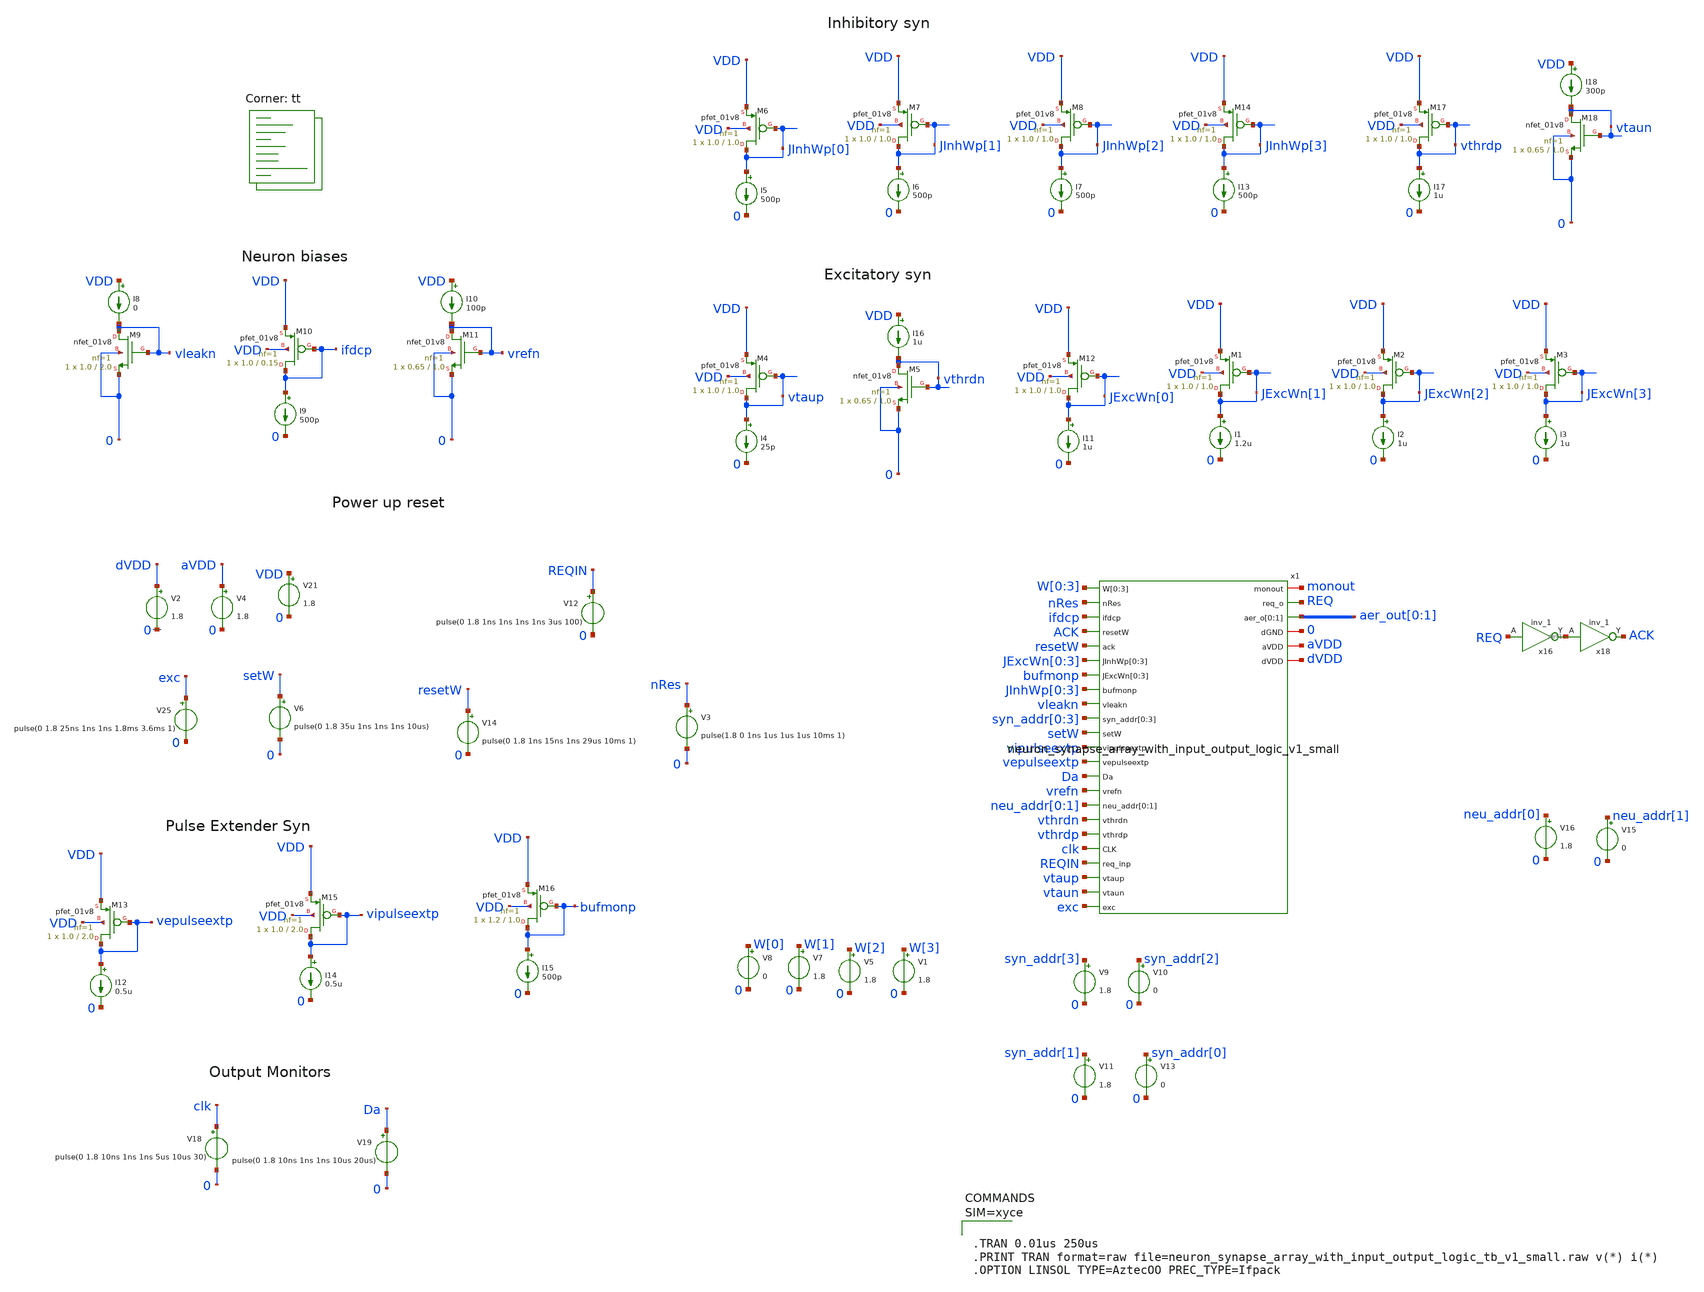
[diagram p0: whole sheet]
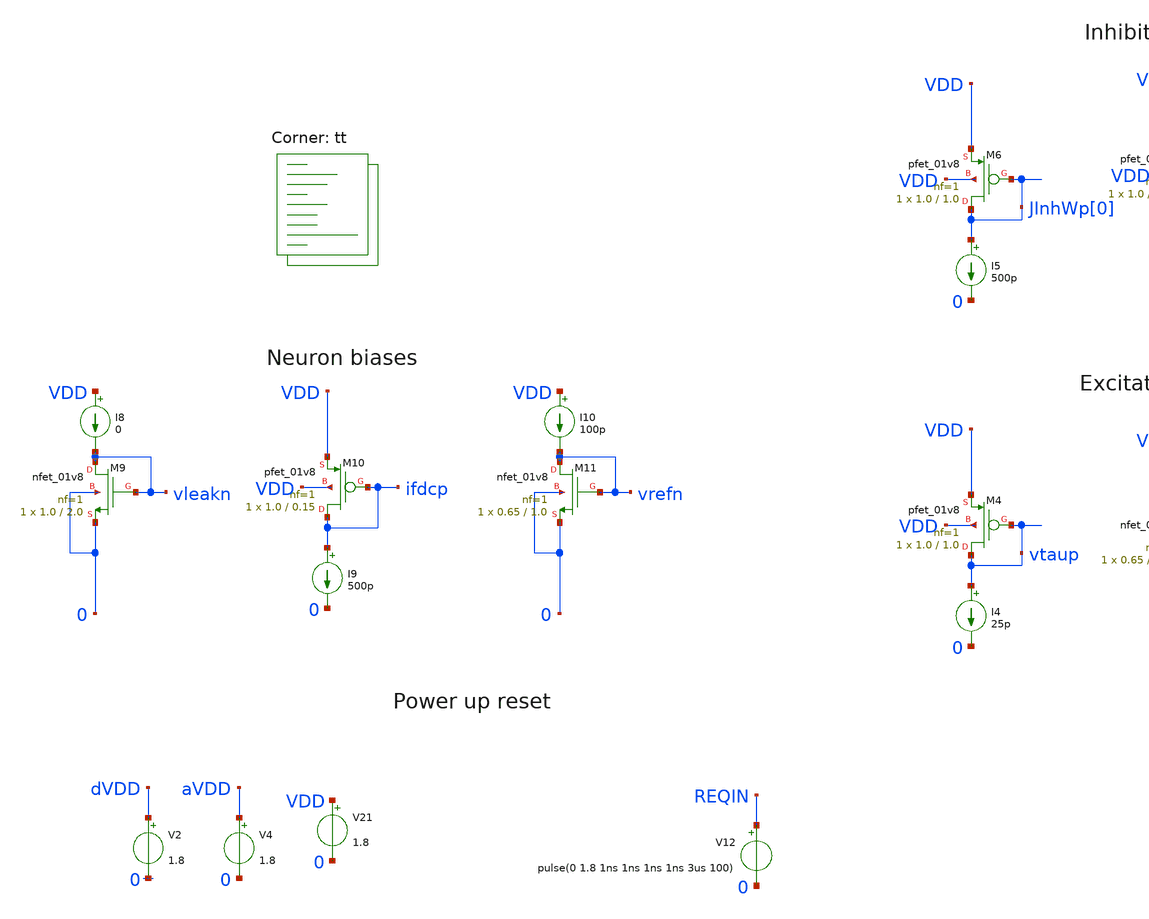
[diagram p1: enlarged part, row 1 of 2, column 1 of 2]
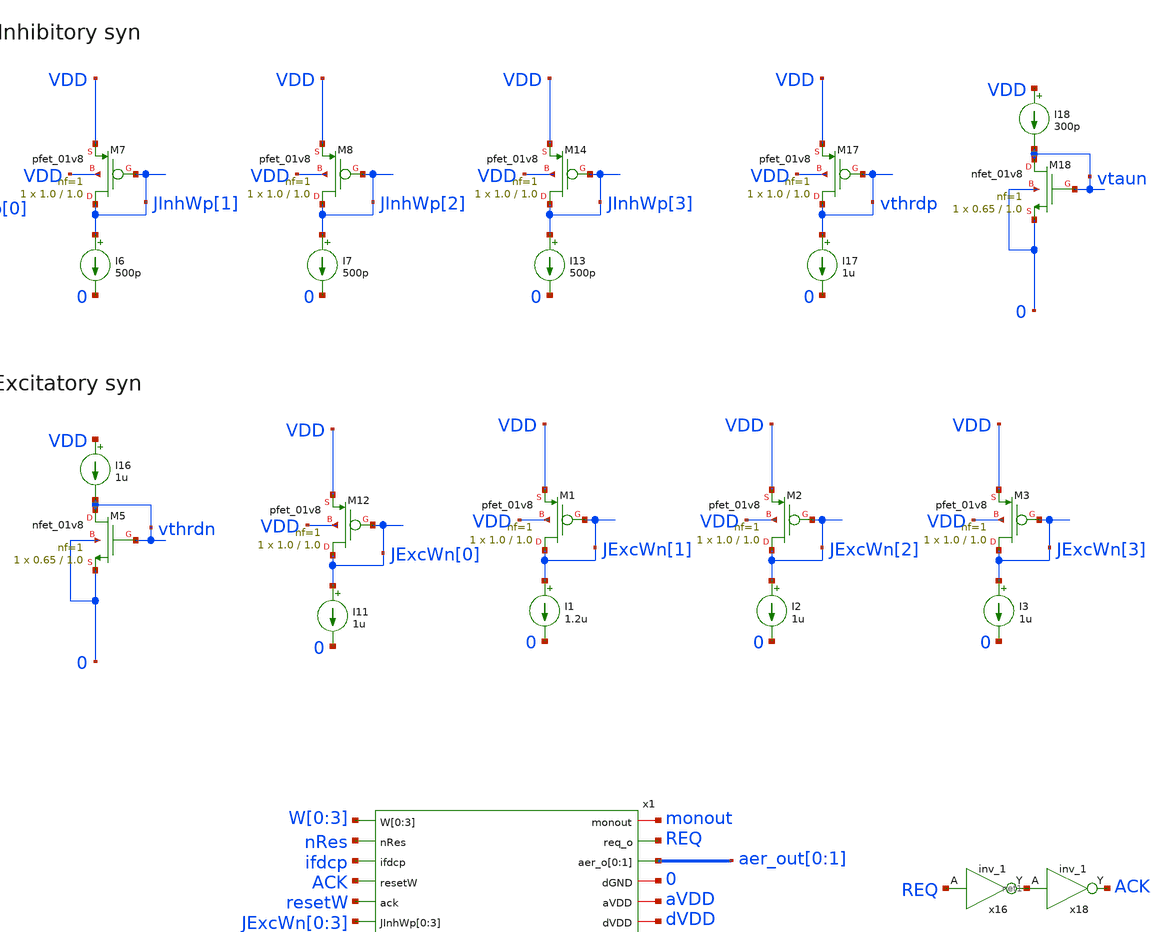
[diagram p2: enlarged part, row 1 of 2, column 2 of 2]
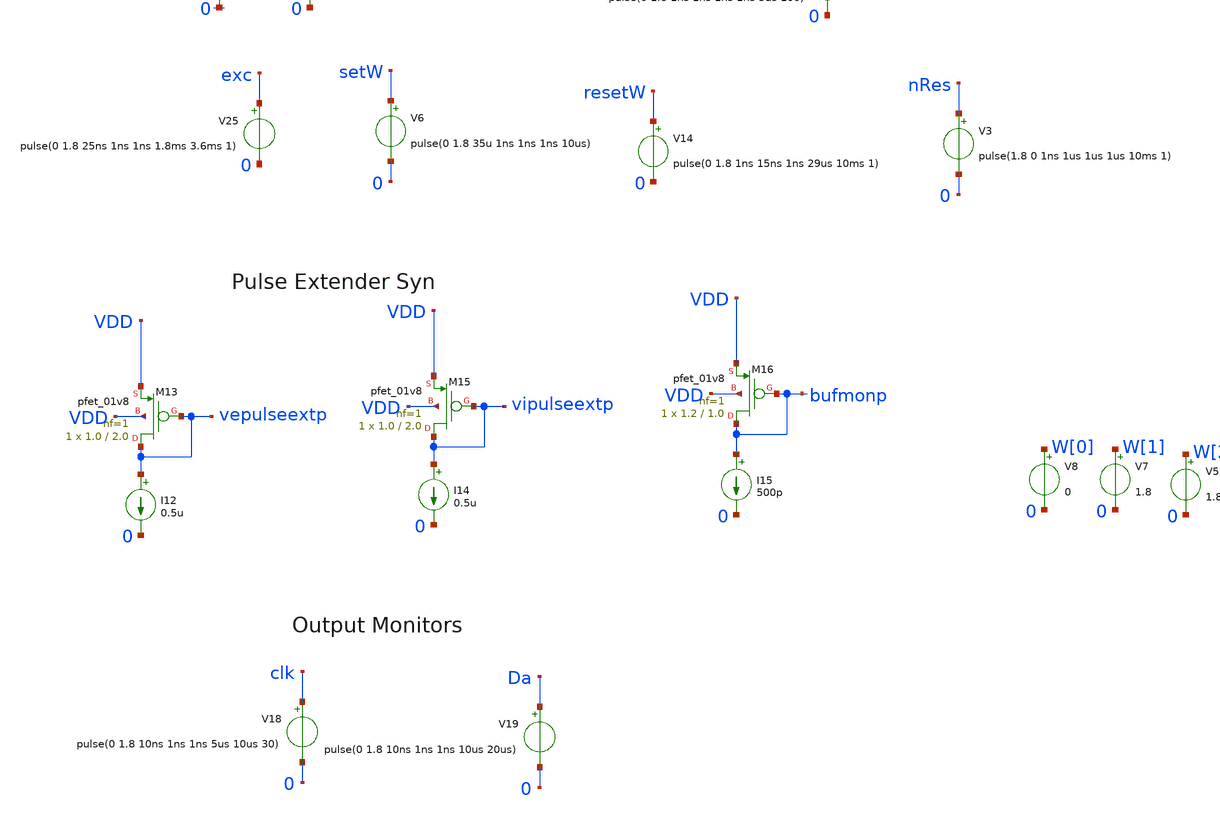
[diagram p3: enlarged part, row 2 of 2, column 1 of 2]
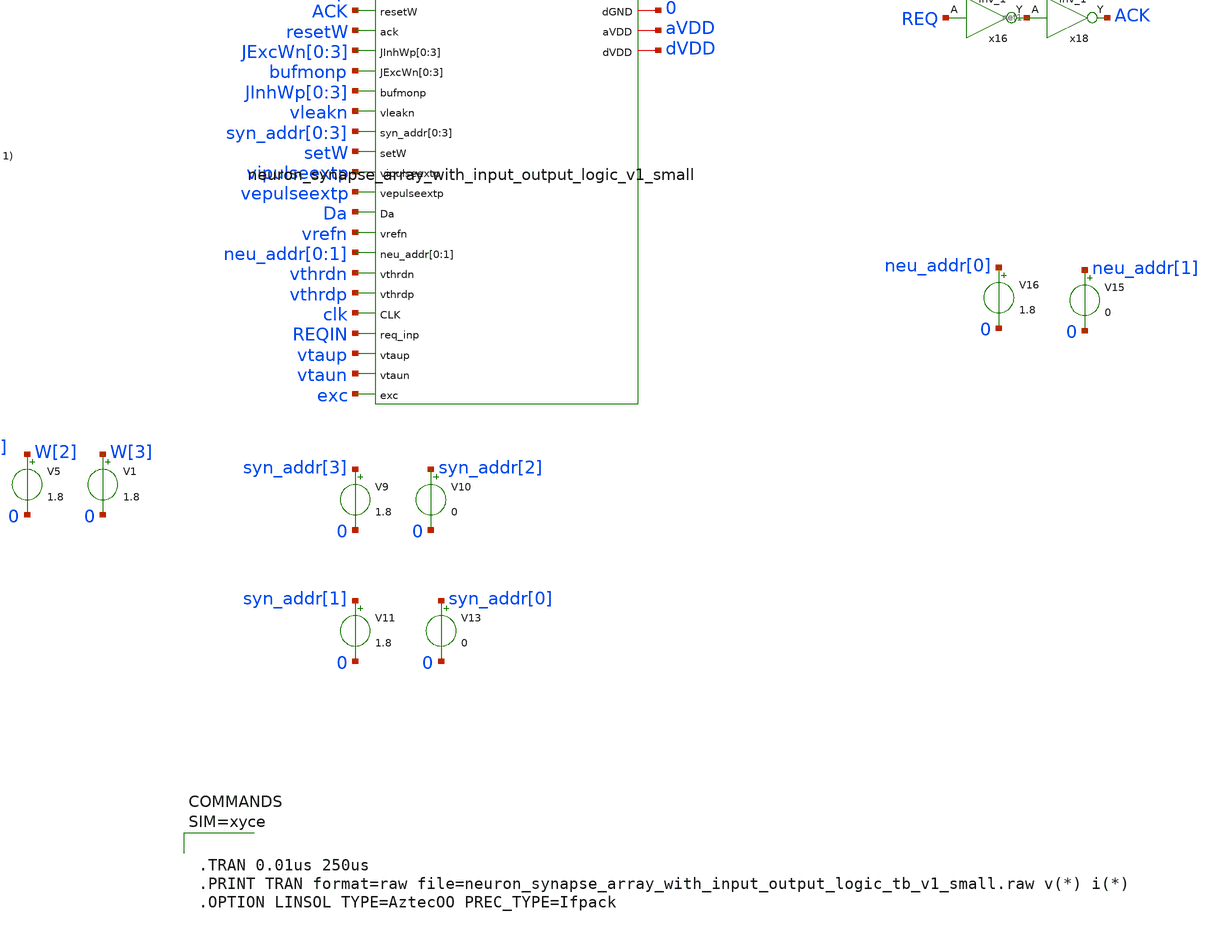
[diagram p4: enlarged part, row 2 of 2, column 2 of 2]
** sch_path: design/xschem/neuron_synapse_array_with_input_output_logic_v1_small_tb.sch
**.subckt neuron_synapse_array_with_input_output_logic_v1_small_tb
V2 dVDD 0 1.8
V12 REQIN 0 pulse(0 1.8 1ns 1ns 1ns 1ns 3us 100)
V4 aVDD 0 1.8
x16 REQ 0 0 VDD VDD net1 sky130_fd_sc_hd__inv_1
x18 net1 0 0 VDD VDD ACK sky130_fd_sc_hd__inv_1
V21 VDD 0 1.8
I8 VDD vleakn 0
XM9 vleakn vleakn 0 0 sky130_fd_pr__nfet_01v8 L=2.0 W=1.0 nf=1 ad='int((nf+1)/2) * W/nf * 0.29' as='int((nf+2)/2) * W/nf * 0.29'
+ pd='2*int((nf+1)/2) * (W/nf + 0.29)' ps='2*int((nf+2)/2) * (W/nf + 0.29)' nrd='0.29 / W' nrs='0.29 / W'
+ sa=0 sb=0 sd=0 mult=1 m=1
XM10 ifdcp ifdcp VDD VDD sky130_fd_pr__pfet_01v8 L=0.15 W=1.0 nf=1 ad='int((nf+1)/2) * W/nf * 0.29' as='int((nf+2)/2) * W/nf * 0.29'
+ pd='2*int((nf+1)/2) * (W/nf + 0.29)' ps='2*int((nf+2)/2) * (W/nf + 0.29)' nrd='0.29 / W' nrs='0.29 / W'
+ sa=0 sb=0 sd=0 mult=1 m=1
I9 ifdcp 0 500p
I10 VDD vrefn 100p
XM11 vrefn vrefn 0 0 sky130_fd_pr__nfet_01v8 L=1.0 W=0.65 nf=1 ad='int((nf+1)/2) * W/nf * 0.29' as='int((nf+2)/2) * W/nf * 0.29'
+ pd='2*int((nf+1)/2) * (W/nf + 0.29)' ps='2*int((nf+2)/2) * (W/nf + 0.29)' nrd='0.29 / W' nrs='0.29 / W'
+ sa=0 sb=0 sd=0 mult=1 m=1
XM13 vepulseextp vepulseextp VDD VDD sky130_fd_pr__pfet_01v8 L=2.0 W=1.0 nf=1 ad='int((nf+1)/2) * W/nf * 0.29'
+ as='int((nf+2)/2) * W/nf * 0.29' pd='2*int((nf+1)/2) * (W/nf + 0.29)' ps='2*int((nf+2)/2) * (W/nf + 0.29)'
+ nrd='0.29 / W' nrs='0.29 / W' sa=0 sb=0 sd=0 mult=1 m=1
I12 vepulseextp 0 0.5u
XM15 vipulseextp vipulseextp VDD VDD sky130_fd_pr__pfet_01v8 L=2.0 W=1.0 nf=1 ad='int((nf+1)/2) * W/nf * 0.29'
+ as='int((nf+2)/2) * W/nf * 0.29' pd='2*int((nf+1)/2) * (W/nf + 0.29)' ps='2*int((nf+2)/2) * (W/nf + 0.29)'
+ nrd='0.29 / W' nrs='0.29 / W' sa=0 sb=0 sd=0 mult=1 m=1
I14 vipulseextp 0 0.5u
XM16 bufmonp bufmonp VDD VDD sky130_fd_pr__pfet_01v8 L=1.0 W=1.2 nf=1 ad='int((nf+1)/2) * W/nf * 0.29'
+ as='int((nf+2)/2) * W/nf * 0.29' pd='2*int((nf+1)/2) * (W/nf + 0.29)' ps='2*int((nf+2)/2) * (W/nf + 0.29)'
+ nrd='0.29 / W' nrs='0.29 / W' sa=0 sb=0 sd=0 mult=1 m=1
I15 bufmonp 0 500p
x1 W[0] W[1] W[2] W[3] nRes monout REQ ifdcp ACK resetW JExcWn[0] JExcWn[1] JExcWn[2] JExcWn[3]
+ aer_out[0] aer_out[1] bufmonp bufmonp bufmonp bufmonp JInhWp[0] vleakn syn_addr[0] syn_addr[1] syn_addr[2]
+ syn_addr[3] setW vipulseextp vepulseextp Da vrefn neu_addr[0] neu_addr[1] vthrdn vthrdp clk REQIN vtaup vtaun
+ exc 0 aVDD dVDD neuron_synapse_array_with_input_output_logic_v1_small
XM12 JExcWn[0] JExcWn[0] VDD VDD sky130_fd_pr__pfet_01v8 L=1.0 W=1.0 nf=1 ad='int((nf+1)/2) * W/nf * 0.29'
+ as='int((nf+2)/2) * W/nf * 0.29' pd='2*int((nf+1)/2) * (W/nf + 0.29)' ps='2*int((nf+2)/2) * (W/nf + 0.29)'
+ nrd='0.29 / W' nrs='0.29 / W' sa=0 sb=0 sd=0 mult=1 m=1
I11 JExcWn[0] 0 1u
XM1 JExcWn[1] JExcWn[1] VDD VDD sky130_fd_pr__pfet_01v8 L=1.0 W=1.0 nf=1 ad='int((nf+1)/2) * W/nf * 0.29'
+ as='int((nf+2)/2) * W/nf * 0.29' pd='2*int((nf+1)/2) * (W/nf + 0.29)' ps='2*int((nf+2)/2) * (W/nf + 0.29)'
+ nrd='0.29 / W' nrs='0.29 / W' sa=0 sb=0 sd=0 mult=1 m=1
I1 JExcWn[1] 0 1.2u
XM2 JExcWn[2] JExcWn[2] VDD VDD sky130_fd_pr__pfet_01v8 L=1.0 W=1.0 nf=1 ad='int((nf+1)/2) * W/nf * 0.29'
+ as='int((nf+2)/2) * W/nf * 0.29' pd='2*int((nf+1)/2) * (W/nf + 0.29)' ps='2*int((nf+2)/2) * (W/nf + 0.29)'
+ nrd='0.29 / W' nrs='0.29 / W' sa=0 sb=0 sd=0 mult=1 m=1
I2 JExcWn[2] 0 1u
XM3 JExcWn[3] JExcWn[3] VDD VDD sky130_fd_pr__pfet_01v8 L=1.0 W=1.0 nf=1 ad='int((nf+1)/2) * W/nf * 0.29'
+ as='int((nf+2)/2) * W/nf * 0.29' pd='2*int((nf+1)/2) * (W/nf + 0.29)' ps='2*int((nf+2)/2) * (W/nf + 0.29)'
+ nrd='0.29 / W' nrs='0.29 / W' sa=0 sb=0 sd=0 mult=1 m=1
I3 JExcWn[3] 0 1u
XM4 vtaup vtaup VDD VDD sky130_fd_pr__pfet_01v8 L=1.0 W=1.0 nf=1 ad='int((nf+1)/2) * W/nf * 0.29' as='int((nf+2)/2) * W/nf * 0.29'
+ pd='2*int((nf+1)/2) * (W/nf + 0.29)' ps='2*int((nf+2)/2) * (W/nf + 0.29)' nrd='0.29 / W' nrs='0.29 / W'
+ sa=0 sb=0 sd=0 mult=1 m=1
I4 vtaup 0 25p
I16 VDD vthrdn 1u
XM5 vthrdn vthrdn 0 0 sky130_fd_pr__nfet_01v8 L=1.0 W=0.65 nf=1 ad='int((nf+1)/2) * W/nf * 0.29' as='int((nf+2)/2) * W/nf * 0.29'
+ pd='2*int((nf+1)/2) * (W/nf + 0.29)' ps='2*int((nf+2)/2) * (W/nf + 0.29)' nrd='0.29 / W' nrs='0.29 / W'
+ sa=0 sb=0 sd=0 mult=1 m=1
XM6 JInhWp[0] JInhWp[0] VDD VDD sky130_fd_pr__pfet_01v8 L=1.0 W=1.0 nf=1 ad='int((nf+1)/2) * W/nf * 0.29'
+ as='int((nf+2)/2) * W/nf * 0.29' pd='2*int((nf+1)/2) * (W/nf + 0.29)' ps='2*int((nf+2)/2) * (W/nf + 0.29)'
+ nrd='0.29 / W' nrs='0.29 / W' sa=0 sb=0 sd=0 mult=1 m=1
I5 JInhWp[0] 0 500p
XM7 JInhWp[1] JInhWp[1] VDD VDD sky130_fd_pr__pfet_01v8 L=1.0 W=1.0 nf=1 ad='int((nf+1)/2) * W/nf * 0.29'
+ as='int((nf+2)/2) * W/nf * 0.29' pd='2*int((nf+1)/2) * (W/nf + 0.29)' ps='2*int((nf+2)/2) * (W/nf + 0.29)'
+ nrd='0.29 / W' nrs='0.29 / W' sa=0 sb=0 sd=0 mult=1 m=1
I6 JInhWp[1] 0 500p
XM8 JInhWp[2] JInhWp[2] VDD VDD sky130_fd_pr__pfet_01v8 L=1.0 W=1.0 nf=1 ad='int((nf+1)/2) * W/nf * 0.29'
+ as='int((nf+2)/2) * W/nf * 0.29' pd='2*int((nf+1)/2) * (W/nf + 0.29)' ps='2*int((nf+2)/2) * (W/nf + 0.29)'
+ nrd='0.29 / W' nrs='0.29 / W' sa=0 sb=0 sd=0 mult=1 m=1
I7 JInhWp[2] 0 500p
XM14 JInhWp[3] JInhWp[3] VDD VDD sky130_fd_pr__pfet_01v8 L=1.0 W=1.0 nf=1 ad='int((nf+1)/2) * W/nf * 0.29'
+ as='int((nf+2)/2) * W/nf * 0.29' pd='2*int((nf+1)/2) * (W/nf + 0.29)' ps='2*int((nf+2)/2) * (W/nf + 0.29)'
+ nrd='0.29 / W' nrs='0.29 / W' sa=0 sb=0 sd=0 mult=1 m=1
I13 JInhWp[3] 0 500p
XM17 vthrdp vthrdp VDD VDD sky130_fd_pr__pfet_01v8 L=1.0 W=1.0 nf=1 ad='int((nf+1)/2) * W/nf * 0.29'
+ as='int((nf+2)/2) * W/nf * 0.29' pd='2*int((nf+1)/2) * (W/nf + 0.29)' ps='2*int((nf+2)/2) * (W/nf + 0.29)'
+ nrd='0.29 / W' nrs='0.29 / W' sa=0 sb=0 sd=0 mult=1 m=1
I17 vthrdp 0 1u
I18 VDD vtaun 300p
XM18 vtaun vtaun 0 0 sky130_fd_pr__nfet_01v8 L=1.0 W=0.65 nf=1 ad='int((nf+1)/2) * W/nf * 0.29' as='int((nf+2)/2) * W/nf * 0.29'
+ pd='2*int((nf+1)/2) * (W/nf + 0.29)' ps='2*int((nf+2)/2) * (W/nf + 0.29)' nrd='0.29 / W' nrs='0.29 / W'
+ sa=0 sb=0 sd=0 mult=1 m=1
V25 exc 0 pulse(0 1.8 25ns 1ns 1ns 1.8ms 3.6ms 1)
V3 nRes 0 pulse(1.8 0 1ns 1us 1us 1us 10ms 1)
V6 setW 0 pulse(0 1.8 35u 1ns 1ns 1ns 10us)
V14 resetW 0 pulse(0 1.8 1ns 15ns 1ns 29us 10ms 1)
V18 clk 0 pulse(0 1.8 10ns 1ns 1ns 5us 10us 30)
V19 Da 0 pulse(0 1.8 10ns 1ns 1ns 10us 20us)
V1 W[3] 0 1.8
V5 W[2] 0 1.8
V7 W[1] 0 1.8
V8 W[0] 0 0
V9 syn_addr[3] 0 1.8
V10 syn_addr[2] 0 0
V11 syn_addr[1] 0 1.8
V13 syn_addr[0] 0 0
V15 neu_addr[1] 0 0
V16 neu_addr[0] 0 1.8
**** begin user architecture code


* Standard cell simulation files
.include $::SKYWATER_STDCELLS/sky130_fd_sc_hd.spice


.lib $::SKYWATER_MODELS/sky130.lib.spice tt



**** end user architecture code
**.ends
.end
